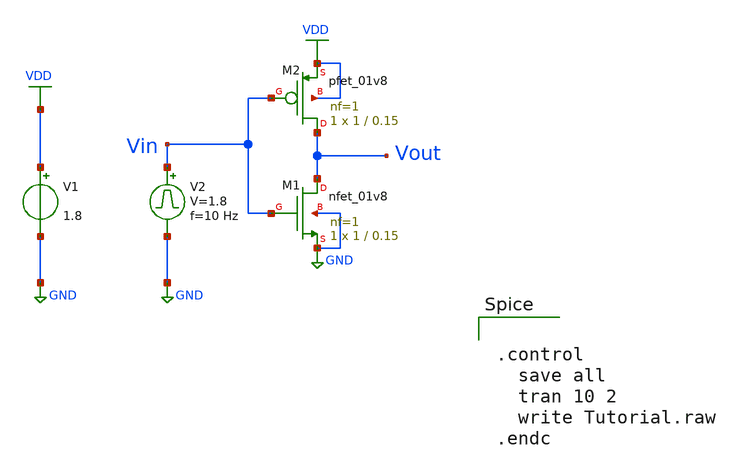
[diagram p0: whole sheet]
** sch_path: Tutorial.sch
**.subckt Tutorial
XM1 Vout Vin GND GND sky130_fd_pr__nfet_01v8 L=0.15 W=1 nf=1 ad='int((nf+1)/2) * W/nf * 0.29' as='int((nf+2)/2) * W/nf * 0.29'
+ pd='2*int((nf+1)/2) * (W/nf + 0.29)' ps='2*int((nf+2)/2) * (W/nf + 0.29)' nrd='0.29 / W' nrs='0.29 / W'
+ sa=0 sb=0 sd=0 mult=1 m=1
XM2 Vout Vin VDD VDD sky130_fd_pr__pfet_01v8 L=0.15 W=1 nf=1 ad='int((nf+1)/2) * W/nf * 0.29' as='int((nf+2)/2) * W/nf * 0.29'
+ pd='2*int((nf+1)/2) * (W/nf + 0.29)' ps='2*int((nf+2)/2) * (W/nf + 0.29)' nrd='0.29 / W' nrs='0.29 / W'
+ sa=0 sb=0 sd=0 mult=1 m=1
V1 VDD GND 1.8
V2 Vin GND pulse 0 1.8 '0.495/ 10 ' '0.01/10 ' '0.01/10 ' '0.49/10 ' '1/10 '
**** begin user architecture code


.lib /classes/c2s2/pdks/volare/sky130/versions/fa87f8f4bbcc7255b6f0c0fb506960f531ae2392/sky130A/libs.tech/ngspice/sky130.lib.spice tt




.control
  save all
  tran 10 2
  write Tutorial.raw
.endc


**** end user architecture code
**.ends
.GLOBAL GND
.GLOBAL VDD
.end
